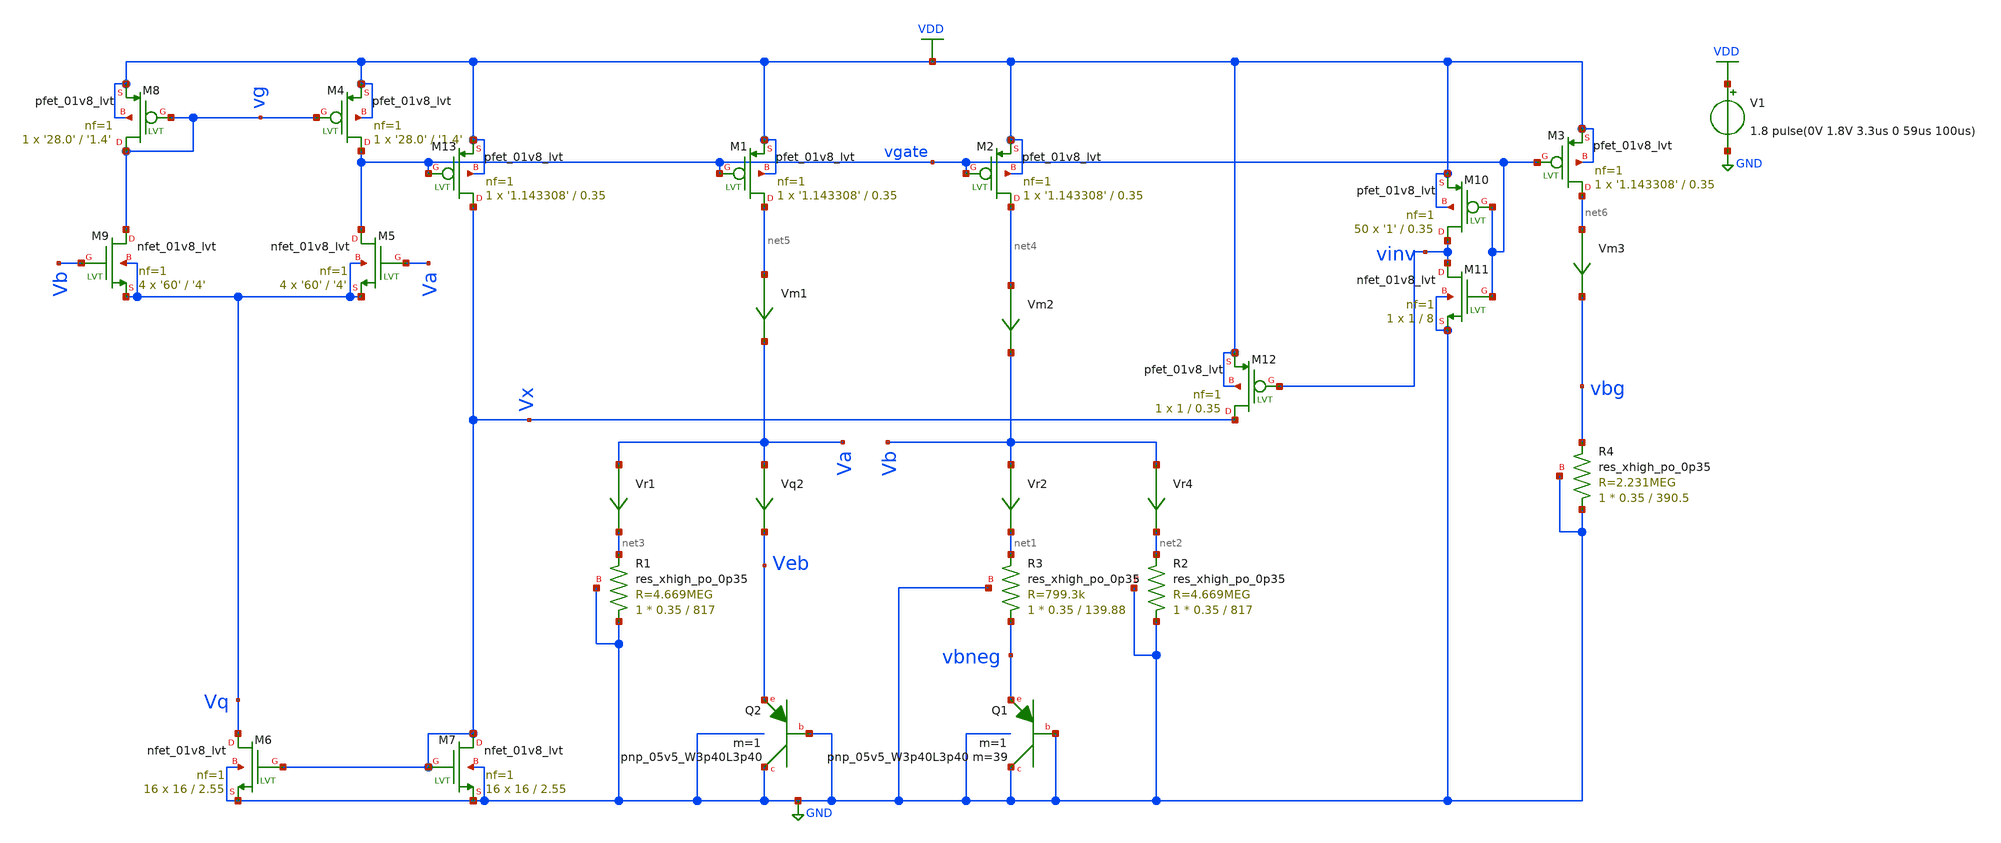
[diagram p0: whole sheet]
** sch_path: schematics/tsmc_bandgap_real_midquarter.sch
**.subckt tsmc_bandgap_real_midquarter
V1 VDD GND 1.8 pulse(0V 1.8V 3.3us 0 59us 100us)
XQ2 GND GND Veb sky130_fd_pr__pnp_05v5_W3p40L3p40 m=1
Vr4 Vb net2 0
.save i(vr4)
Vr2 Vb net1 0
.save i(vr2)
Vm1 net5 Va 0
.save i(vm1)
Vm2 net4 Vb 0
.save i(vm2)
Vm3 net6 vbg 0
.save i(vm3)
Vr1 Va net3 0
.save i(vr1)
Vq2 Va Veb 0
.save i(vq2)
XQ1 GND GND vbneg sky130_fd_pr__pnp_05v5_W3p40L3p40 m=39 m=1
XM4 vgate vg VDD VDD sky130_fd_pr__pfet_01v8_lvt L='1.4' W='28.0' nf=1 ad='int((nf+1)/2) * W/nf * 0.29'
+ as='int((nf+2)/2) * W/nf * 0.29' pd='2*int((nf+1)/2) * (W/nf + 0.29)' ps='2*int((nf+2)/2) * (W/nf + 0.29)'
+ nrd='0.29 / W' nrs='0.29 / W' sa=0 sb=0 sd=0 mult=1 m=1
XM5 vgate Va Vq Vq sky130_fd_pr__nfet_01v8_lvt L='4' W='60' nf=1 ad='int((nf+1)/2) * W/nf * 0.29' as='int((nf+2)/2) * W/nf * 0.29'
+ pd='2*int((nf+1)/2) * (W/nf + 0.29)' ps='2*int((nf+2)/2) * (W/nf + 0.29)' nrd='0.29 / W' nrs='0.29 / W'
+ sa=0 sb=0 sd=0 mult=4 m=4
XM6 Vq Vx GND GND sky130_fd_pr__nfet_01v8_lvt L=2.55 W=16 nf=1 ad='int((nf+1)/2) * W/nf * 0.29' as='int((nf+2)/2) * W/nf * 0.29'
+ pd='2*int((nf+1)/2) * (W/nf + 0.29)' ps='2*int((nf+2)/2) * (W/nf + 0.29)' nrd='0.29 / W' nrs='0.29 / W'
+ sa=0 sb=0 sd=0 mult=16 m=16
XM8 vg vg VDD VDD sky130_fd_pr__pfet_01v8_lvt L='1.4' W='28.0' nf=1 ad='int((nf+1)/2) * W/nf * 0.29'
+ as='int((nf+2)/2) * W/nf * 0.29' pd='2*int((nf+1)/2) * (W/nf + 0.29)' ps='2*int((nf+2)/2) * (W/nf + 0.29)'
+ nrd='0.29 / W' nrs='0.29 / W' sa=0 sb=0 sd=0 mult=1 m=1
XM9 vg Vb Vq Vq sky130_fd_pr__nfet_01v8_lvt L='4' W='60' nf=1 ad='int((nf+1)/2) * W/nf * 0.29' as='int((nf+2)/2) * W/nf * 0.29'
+ pd='2*int((nf+1)/2) * (W/nf + 0.29)' ps='2*int((nf+2)/2) * (W/nf + 0.29)' nrd='0.29 / W' nrs='0.29 / W'
+ sa=0 sb=0 sd=0 mult=4 m=4
XM10 vinv vgate VDD VDD sky130_fd_pr__pfet_01v8_lvt L=0.35 W='1' nf=1 ad='int((nf+1)/2) * W/nf * 0.29'
+ as='int((nf+2)/2) * W/nf * 0.29' pd='2*int((nf+1)/2) * (W/nf + 0.29)' ps='2*int((nf+2)/2) * (W/nf + 0.29)'
+ nrd='0.29 / W' nrs='0.29 / W' sa=0 sb=0 sd=0 mult=50 m=50
XM11 vinv vgate GND GND sky130_fd_pr__nfet_01v8_lvt L=8 W=1 nf=1 ad='int((nf+1)/2) * W/nf * 0.29' as='int((nf+2)/2) * W/nf * 0.29'
+ pd='2*int((nf+1)/2) * (W/nf + 0.29)' ps='2*int((nf+2)/2) * (W/nf + 0.29)' nrd='0.29 / W' nrs='0.29 / W'
+ sa=0 sb=0 sd=0 mult=1 m=1
XM12 Vx vinv VDD VDD sky130_fd_pr__pfet_01v8_lvt L=0.35 W=1 nf=1 ad='int((nf+1)/2) * W/nf * 0.29' as='int((nf+2)/2) * W/nf * 0.29'
+ pd='2*int((nf+1)/2) * (W/nf + 0.29)' ps='2*int((nf+2)/2) * (W/nf + 0.29)' nrd='0.29 / W' nrs='0.29 / W'
+ sa=0 sb=0 sd=0 mult=1 m=1
XM7 Vx Vx GND GND sky130_fd_pr__nfet_01v8_lvt L=2.55 W=16 nf=1 ad='int((nf+1)/2) * W/nf * 0.29' as='int((nf+2)/2) * W/nf * 0.29'
+ pd='2*int((nf+1)/2) * (W/nf + 0.29)' ps='2*int((nf+2)/2) * (W/nf + 0.29)' nrd='0.29 / W' nrs='0.29 / W'
+ sa=0 sb=0 sd=0 mult=16 m=16
XM13 Vx vgate VDD VDD sky130_fd_pr__pfet_01v8_lvt L=0.35 W='1.143308' nf=1 ad='int((nf+1)/2) * W/nf * 0.29'
+ as='int((nf+2)/2) * W/nf * 0.29' pd='2*int((nf+1)/2) * (W/nf + 0.29)' ps='2*int((nf+2)/2) * (W/nf + 0.29)'
+ nrd='0.29 / W' nrs='0.29 / W' sa=0 sb=0 sd=0 mult=1 m=1
XM1 net5 vgate VDD VDD sky130_fd_pr__pfet_01v8_lvt L=0.35 W='1.143308' nf=1 ad='int((nf+1)/2) * W/nf * 0.29'
+ as='int((nf+2)/2) * W/nf * 0.29' pd='2*int((nf+1)/2) * (W/nf + 0.29)' ps='2*int((nf+2)/2) * (W/nf + 0.29)'
+ nrd='0.29 / W' nrs='0.29 / W' sa=0 sb=0 sd=0 mult=1 m=1
XM2 net4 vgate VDD VDD sky130_fd_pr__pfet_01v8_lvt L=0.35 W='1.143308' nf=1 ad='int((nf+1)/2) * W/nf * 0.29'
+ as='int((nf+2)/2) * W/nf * 0.29' pd='2*int((nf+1)/2) * (W/nf + 0.29)' ps='2*int((nf+2)/2) * (W/nf + 0.29)'
+ nrd='0.29 / W' nrs='0.29 / W' sa=0 sb=0 sd=0 mult=1 m=1
XM3 net6 vgate VDD VDD sky130_fd_pr__pfet_01v8_lvt L=0.35 W='1.143308' nf=1 ad='int((nf+1)/2) * W/nf * 0.29'
+ as='int((nf+2)/2) * W/nf * 0.29' pd='2*int((nf+1)/2) * (W/nf + 0.29)' ps='2*int((nf+2)/2) * (W/nf + 0.29)'
+ nrd='0.29 / W' nrs='0.29 / W' sa=0 sb=0 sd=0 mult=1 m=1
XR1 GND net3 GND sky130_fd_pr__res_xhigh_po_0p35 L=817 mult=1 m=1
XR2 GND net2 GND sky130_fd_pr__res_xhigh_po_0p35 L=817 mult=1 m=1
XR3 vbneg net1 GND sky130_fd_pr__res_xhigh_po_0p35 L=139.88 mult=1 m=1
XR4 GND vbg GND sky130_fd_pr__res_xhigh_po_0p35 L=390.5 mult=1 m=1
**** begin user architecture code

.include $::SKYWATER_MODELS/cells/nfet_01v8/sky130_fd_pr__nfet_01v8__tt.corner.spice
.include $::SKYWATER_MODELS/cells/nfet_01v8_lvt/sky130_fd_pr__nfet_01v8_lvt__tt.corner.spice
.include $::SKYWATER_MODELS/cells/pfet_01v8/sky130_fd_pr__pfet_01v8__tt.corner.spice
.include $::SKYWATER_MODELS/cells/nfet_03v3_nvt/sky130_fd_pr__nfet_03v3_nvt__tt.corner.spice
.include $::SKYWATER_MODELS/cells/nfet_05v0_nvt/sky130_fd_pr__nfet_05v0_nvt__tt.corner.spice
.include $::SKYWATER_MODELS/cells/esd_nfet_01v8/sky130_fd_pr__esd_nfet_01v8__tt.corner.spice
.include $::SKYWATER_MODELS/cells/pfet_01v8_lvt/sky130_fd_pr__pfet_01v8_lvt__tt.corner.spice
.include $::SKYWATER_MODELS/cells/pfet_01v8_hvt/sky130_fd_pr__pfet_01v8_hvt__tt.corner.spice
.include $::SKYWATER_MODELS/cells/esd_pfet_g5v0d10v5/sky130_fd_pr__esd_pfet_g5v0d10v5__tt.corner.spice
.include $::SKYWATER_MODELS/cells/pfet_g5v0d10v5/sky130_fd_pr__pfet_g5v0d10v5__tt.corner.spice
.include $::SKYWATER_MODELS/cells/pfet_g5v0d16v0/sky130_fd_pr__pfet_g5v0d16v0__tt.corner.spice
.include $::SKYWATER_MODELS/cells/nfet_g5v0d10v5/sky130_fd_pr__nfet_g5v0d10v5__tt.corner.spice
.include $::SKYWATER_MODELS/cells/nfet_g5v0d16v0/sky130_fd_pr__nfet_g5v0d16v0__tt_discrete.corner.spice
.include $::SKYWATER_MODELS/cells/esd_nfet_g5v0d10v5/sky130_fd_pr__esd_nfet_g5v0d10v5__tt.corner.spice
.include $::SKYWATER_MODELS/models/corners/tt/nonfet.spice
* Mismatch parameters
.include $::SKYWATER_MODELS/cells/nfet_01v8/sky130_fd_pr__nfet_01v8__mismatch.corner.spice
.include $::SKYWATER_MODELS/cells/pfet_01v8/sky130_fd_pr__pfet_01v8__mismatch.corner.spice
.include $::SKYWATER_MODELS/cells/nfet_01v8_lvt/sky130_fd_pr__nfet_01v8_lvt__mismatch.corner.spice
.include $::SKYWATER_MODELS/cells/pfet_01v8_lvt/sky130_fd_pr__pfet_01v8_lvt__mismatch.corner.spice
.include $::SKYWATER_MODELS/cells/pfet_01v8_hvt/sky130_fd_pr__pfet_01v8_hvt__mismatch.corner.spice
.include $::SKYWATER_MODELS/cells/nfet_g5v0d10v5/sky130_fd_pr__nfet_g5v0d10v5__mismatch.corner.spice
.include $::SKYWATER_MODELS/cells/pfet_g5v0d10v5/sky130_fd_pr__pfet_g5v0d10v5__mismatch.corner.spice
.include $::SKYWATER_MODELS/cells/nfet_05v0_nvt/sky130_fd_pr__nfet_05v0_nvt__mismatch.corner.spice
.include $::SKYWATER_MODELS/cells/nfet_03v3_nvt/sky130_fd_pr__nfet_03v3_nvt__mismatch.corner.spice
* Resistor$::SKYWATER_MODELS/Capacitor
.include $::SKYWATER_MODELS/models/r+c/res_typical__cap_typical.spice
.include $::SKYWATER_MODELS/models/r+c/res_typical__cap_typical__lin.spice
* Special cells
.include $::SKYWATER_MODELS/models/corners/tt/specialized_cells.spice
* All models
.include $::SKYWATER_MODELS/models/all.spice
.include $::SKYWATER_MODELS/cells/pnp_05v5/sky130_fd_pr__pnp_05v5_W3p40L3p40.model.spice
* Corner
.include $::SKYWATER_MODELS/models/corners/tt/rf.spice



.option savecurrents
.param R3val='800k'
.param alpha='1'
.param R2R3ratio='5.8366561*alpha'
.param R2val='R3val*R2R3ratio'
.param R4R2ratio='0.47810041'
.param R4val='R2val*R4R2ratio'
.control
save all  @m.xm1.msky130_fd_pr__pfet_01v8_lvt[gm]  @m.xm2.msky130_fd_pr__pfet_01v8_lvt[gm]
+  @m.xm3.msky130_fd_pr__pfet_01v8_lvt[gm]  @m.xm4.msky130_fd_pr__pfet_01v8_lvt[gm]  @m.xm5.msky130_fd_pr__nfet_01v8_lvt[gm]
+  @m.xm6.msky130_fd_pr__nfet_01v8_lvt[gm]  @m.xm7.msky130_fd_pr__nfet_01v8_lvt[gm]  @m.xm8.msky130_fd_pr__pfet_01v8_lvt[gm]
+  @m.xm9.msky130_fd_pr__nfet_01v8_lvt[gm]  @m.xm13.msky130_fd_pr__pfet_01v8_lvt[gm]

op
write tsmc_bandgap_real_midquarter.raw
let id8=@m.xm8.msky130_fd_pr__pfet_01v8_lvt[id]
let id1=@m.xm1.msky130_fd_pr__pfet_01v8_lvt[id]
let vth5=@m.xm5.msky130_fd_pr__nfet_01v8_lvt[vth]
let vth6=@m.xm6.msky130_fd_pr__nfet_01v8_lvt[vth]
let wm8=@m.xm8.msky130_fd_pr__pfet_01v8_lvt[w]
let mm8=@m.xm8.msky130_fd_pr__pfet_01v8_lvt[m]
let weff8=wm8*mm8
let jd8=id8/weff8
let wm1=@m.xm1.msky130_fd_pr__pfet_01v8_lvt[w]
let mm1=@m.xm1.msky130_fd_pr__pfet_01v8_lvt[m]
let weff1=wm1*mm1
let jd1=id1/weff1
print vbg vgate vg va vb vx vinv vq
.endc


**** end user architecture code
**.ends
.GLOBAL VDD
.GLOBAL GND
.end
